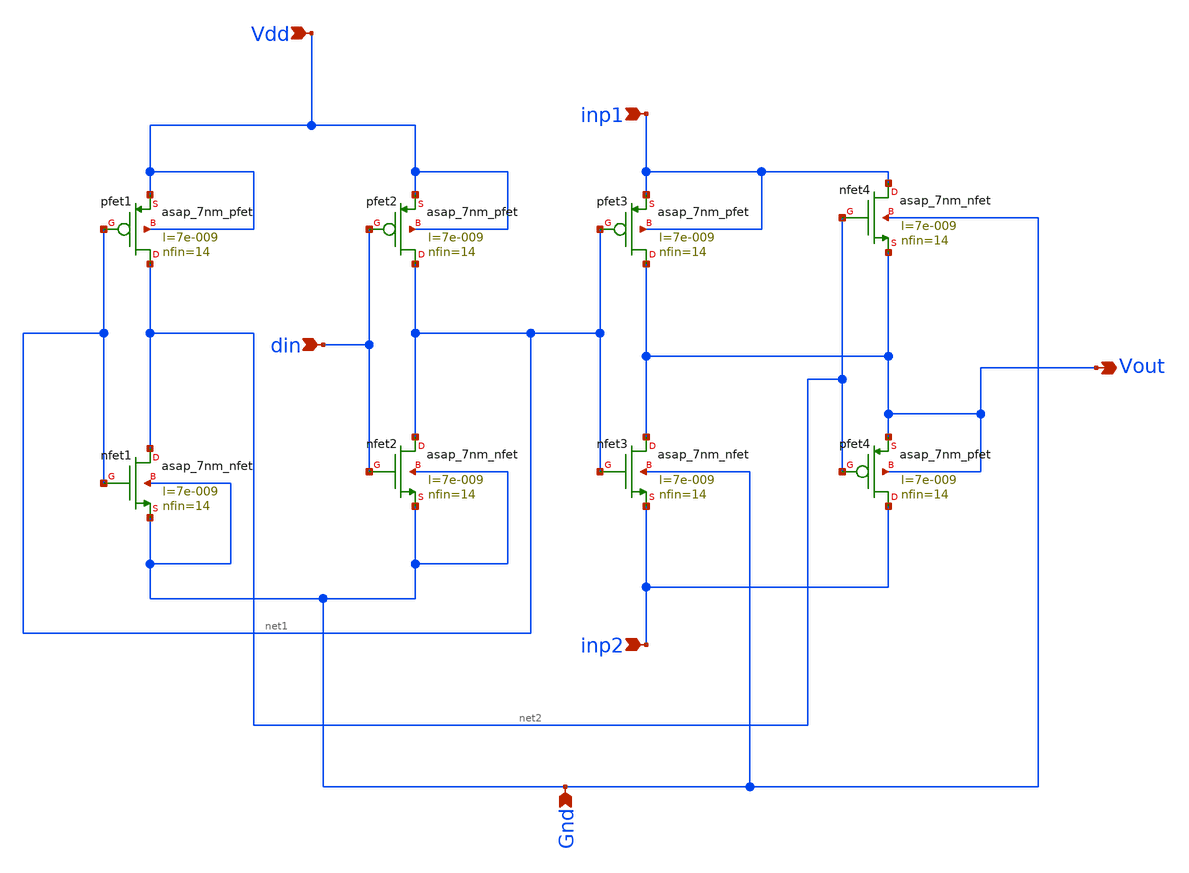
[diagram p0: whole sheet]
** sch_path: Schematics/Switch.sch
**.subckt Switch Vdd inp2 inp1 Vout din Gnd
*.ipin Vdd
*.ipin inp2
*.ipin inp1
*.opin Vout
*.ipin din
*.ipin Gnd
Xnfet1 net2 net1 Gnd Gnd asap_7nm_nfet l=7e-009 nfin=14
Xpfet1 net2 net1 Vdd Vdd asap_7nm_pfet l=7e-009 nfin=14
Xpfet2 net1 din Vdd Vdd asap_7nm_pfet l=7e-009 nfin=14
Xnfet2 net1 din Gnd Gnd asap_7nm_nfet l=7e-009 nfin=14
Xpfet3 Vout net1 inp1 inp1 asap_7nm_pfet l=7e-009 nfin=14
Xnfet3 Vout net1 inp2 Gnd asap_7nm_nfet l=7e-009 nfin=14
Xpfet4 inp2 net2 Vout Vout asap_7nm_pfet l=7e-009 nfin=14
Xnfet4 inp1 net2 Vout Gnd asap_7nm_nfet l=7e-009 nfin=14
**.ends
.end
